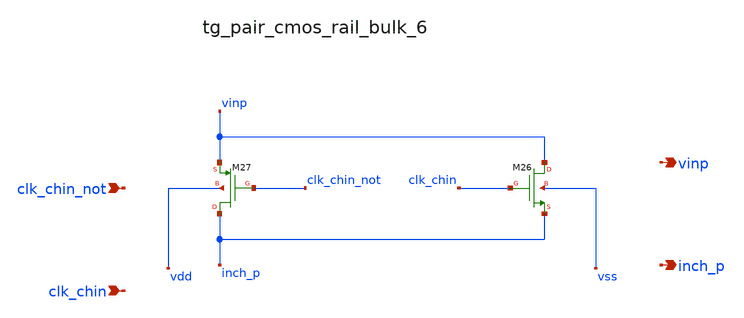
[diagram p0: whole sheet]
** sch_path: analog-db/raw/ia_003_fan_chopper_pf/hier/blocks/tg_pair_cmos_rail_bulk_6.sch
**.subckt tg_pair_cmos_rail_bulk_6 clk_chin_not clk_chin vinp inch_p
*.ipin clk_chin_not
*.ipin clk_chin
*.opin vinp
*.opin inch_p
XM26 vinp clk_chin inch_p vss sg13_lv_nmos w=x_dut_xm26_w l=x_dut_xm26_l ng=1 m=x_dut_xm26_m
XM27 inch_p clk_chin_not vinp vdd sg13_lv_pmos w=x_dut_xm27_w l=x_dut_xm27_l ng=1 m=x_dut_xm27_m
**.ends
.end
